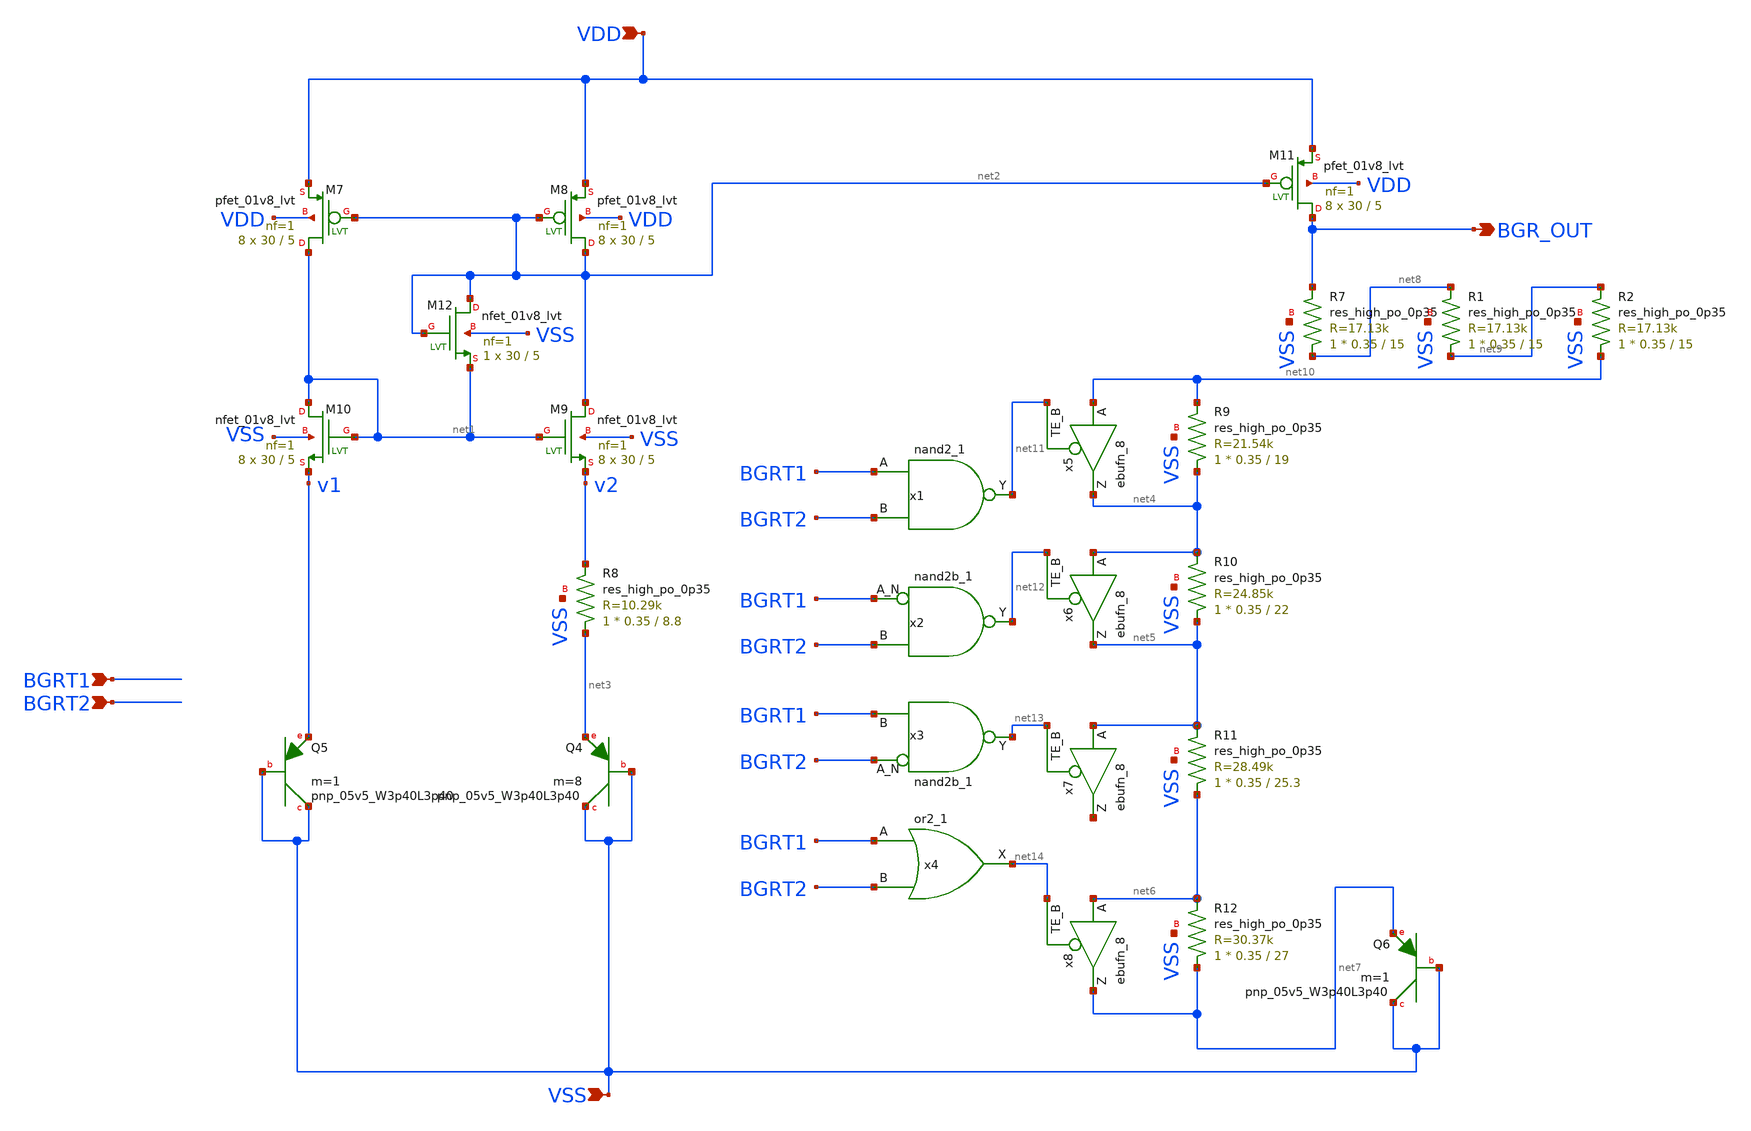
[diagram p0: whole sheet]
** sch_path: xschem/bandgap.sch
**.subckt bandgap BGR_OUT VDD VSS BGRT1 BGRT2
*.opin BGR_OUT
*.ipin VDD
*.ipin VSS
*.ipin BGRT1
*.ipin BGRT2
XM7 net1 net2 VDD VDD sky130_fd_pr__pfet_01v8_lvt L=5 W=30 nf=1 ad='int((nf+1)/2) * W/nf * 0.29' as='int((nf+2)/2) * W/nf * 0.29'
+ pd='2*int((nf+1)/2) * (W/nf + 0.29)' ps='2*int((nf+2)/2) * (W/nf + 0.29)' nrd='0.29 / W' nrs='0.29 / W'
+ sa=0 sb=0 sd=0 mult=8 m=8
XM8 net2 net2 VDD VDD sky130_fd_pr__pfet_01v8_lvt L=5 W=30 nf=1 ad='int((nf+1)/2) * W/nf * 0.29' as='int((nf+2)/2) * W/nf * 0.29'
+ pd='2*int((nf+1)/2) * (W/nf + 0.29)' ps='2*int((nf+2)/2) * (W/nf + 0.29)' nrd='0.29 / W' nrs='0.29 / W'
+ sa=0 sb=0 sd=0 mult=8 m=8
XM9 net2 net1 v2 VSS sky130_fd_pr__nfet_01v8_lvt L=5 W=30 nf=1 ad='int((nf+1)/2) * W/nf * 0.29' as='int((nf+2)/2) * W/nf * 0.29'
+ pd='2*int((nf+1)/2) * (W/nf + 0.29)' ps='2*int((nf+2)/2) * (W/nf + 0.29)' nrd='0.29 / W' nrs='0.29 / W'
+ sa=0 sb=0 sd=0 mult=8 m=8
XM10 net1 net1 v1 VSS sky130_fd_pr__nfet_01v8_lvt L=5 W=30 nf=1 ad='int((nf+1)/2) * W/nf * 0.29' as='int((nf+2)/2) * W/nf * 0.29'
+ pd='2*int((nf+1)/2) * (W/nf + 0.29)' ps='2*int((nf+2)/2) * (W/nf + 0.29)' nrd='0.29 / W' nrs='0.29 / W'
+ sa=0 sb=0 sd=0 mult=8 m=8
XQ4 VSS VSS net3 sky130_fd_pr__pnp_05v5_W3p40L3p40 m=8
XQ5 VSS VSS v1 sky130_fd_pr__pnp_05v5_W3p40L3p40 m=1
XM11 BGR_OUT net2 VDD VDD sky130_fd_pr__pfet_01v8_lvt L=5 W=30 nf=1 ad='int((nf+1)/2) * W/nf * 0.29'
+ as='int((nf+2)/2) * W/nf * 0.29' pd='2*int((nf+1)/2) * (W/nf + 0.29)' ps='2*int((nf+2)/2) * (W/nf + 0.29)'
+ nrd='0.29 / W' nrs='0.29 / W' sa=0 sb=0 sd=0 mult=8 m=8
XR7 net8 BGR_OUT VSS sky130_fd_pr__res_high_po_0p35 L=15 mult=1 m=1
XM12 net2 net2 net1 VSS sky130_fd_pr__nfet_01v8_lvt L=5 W=30 nf=1 ad='int((nf+1)/2) * W/nf * 0.29' as='int((nf+2)/2) * W/nf * 0.29'
+ pd='2*int((nf+1)/2) * (W/nf + 0.29)' ps='2*int((nf+2)/2) * (W/nf + 0.29)' nrd='0.29 / W' nrs='0.29 / W'
+ sa=0 sb=0 sd=0 mult=1 m=1
XR8 net3 v2 VSS sky130_fd_pr__res_high_po_0p35 L=8.8 mult=1 m=1
XR9 net4 net10 VSS sky130_fd_pr__res_high_po_0p35 L=19 mult=1 m=1
XR10 net5 net4 VSS sky130_fd_pr__res_high_po_0p35 L=22 mult=1 m=1
XR11 net6 net5 VSS sky130_fd_pr__res_high_po_0p35 L=25.3 mult=1 m=1
XR12 net7 net6 VSS sky130_fd_pr__res_high_po_0p35 L=27 mult=1 m=1
XQ6 VSS VSS net7 sky130_fd_pr__pnp_05v5_W3p40L3p40 m=1
XR1 net9 net8 VSS sky130_fd_pr__res_high_po_0p35 L=15 mult=1 m=1
XR2 net10 net9 VSS sky130_fd_pr__res_high_po_0p35 L=15 mult=1 m=1
x1 BGRT1 BGRT2 VGND VNB VPB VPWR net11 sky130_fd_sc_hd__nand2_1
x2 BGRT1 BGRT2 VGND VNB VPB VPWR net12 sky130_fd_sc_hd__nand2b_1
x3 BGRT2 BGRT1 VGND VNB VPB VPWR net13 sky130_fd_sc_hd__nand2b_1
x4 BGRT1 BGRT2 VGND VNB VPB VPWR net14 sky130_fd_sc_hd__or2_1
x5 net10 net11 VGND VNB VPB VPWR net4 sky130_fd_sc_hd__ebufn_8
x6 net4 net12 VGND VNB VPB VPWR net5 sky130_fd_sc_hd__ebufn_8
x7 net5 net13 VGND VNB VPB VPWR net15 sky130_fd_sc_hd__ebufn_8
x8 net6 net14 VGND VNB VPB VPWR net7 sky130_fd_sc_hd__ebufn_8
**.ends
.end
